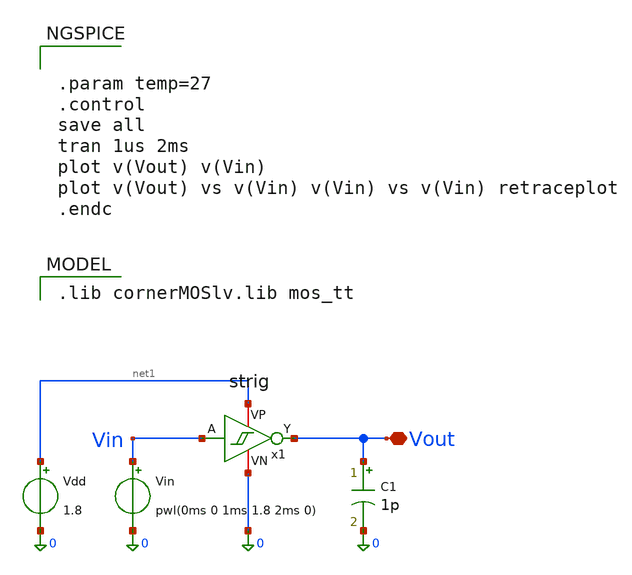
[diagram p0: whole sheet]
** sch_path: xschem/strig_tb.sch
**.subckt strig_tb Vout
*.iopin Vout
Vin Vin 0 pwl(0ms 0 1ms 1.8 2ms 0)
Vdd net1 0 1.8
x1 net1 Vin Vout 0 strig
C1 Vout 0 1p m=1
**** begin user architecture code
 .lib cornerMOSlv.lib mos_tt



.param temp=27
.control
save all
tran 1us 2ms
plot v(Vout) v(Vin)
plot v(Vout) vs v(Vin) v(Vin) vs v(Vin) retraceplot
.endc


**** end user architecture code
**.ends

* expanding   symbol:  strig.sym # of pins=4
** sym_path: xschem/strig.sym
** sch_path: xschem/strig.sch
.subckt strig VP A Y VN
*.iopin VP
*.iopin VN
*.ipin A
*.opin Y
XM1 net1 A VN VN sg13_lv_nmos w=0.15u l=0.13u ng=1 m=1 mm_ok=1
Xq Y A net1 VN sg13_lv_nmos w=0.15u l=0.13u ng=1 m=1 mm_ok=1
XM3 VP Y net1 VN sg13_lv_nmos w=0.15u l=0.13u ng=1 m=1 mm_ok=1
XM4 VN Y net2 VP sg13_lv_pmos w=0.15u l=0.13u ng=1 m=1 mm_ok=1
XM5 Y A net2 VP sg13_lv_pmos w=0.15u l=0.13u ng=1 m=1 mm_ok=1
XM6 net2 A VP VP sg13_lv_pmos w=0.15u l=0.13u ng=1 m=1 mm_ok=1
.ends

.end
